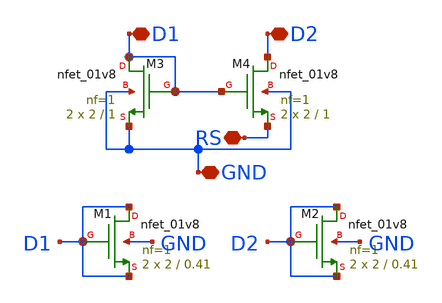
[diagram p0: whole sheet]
** sch_path: block2/xschem/block2.sch
**.subckt block2 RS D1 D2 GND
*.iopin RS
*.iopin D1
*.iopin D2
*.iopin GND
XM3 D1 D1 GND GND sky130_fd_pr__nfet_01v8 L=1 W=2 nf=1 ad='int((nf+1)/2) * W/nf * 0.29' as='int((nf+2)/2) * W/nf * 0.29'
+ pd='2*int((nf+1)/2) * (W/nf + 0.29)' ps='2*int((nf+2)/2) * (W/nf + 0.29)' nrd='0.29 / W' nrs='0.29 / W'
+ sa=0 sb=0 sd=0 mult=2 m=2
XM4 D2 D1 RS GND sky130_fd_pr__nfet_01v8 L=1 W=2 nf=1 ad='int((nf+1)/2) * W/nf * 0.29' as='int((nf+2)/2) * W/nf * 0.29'
+ pd='2*int((nf+1)/2) * (W/nf + 0.29)' ps='2*int((nf+2)/2) * (W/nf + 0.29)' nrd='0.29 / W' nrs='0.29 / W'
+ sa=0 sb=0 sd=0 mult=2 m=2
XM1 D1 D1 D1 GND sky130_fd_pr__nfet_01v8 L=0.41 W=2 nf=1 ad='int((nf+1)/2) * W/nf * 0.29' as='int((nf+2)/2) * W/nf * 0.29'
+ pd='2*int((nf+1)/2) * (W/nf + 0.29)' ps='2*int((nf+2)/2) * (W/nf + 0.29)' nrd='0.29 / W' nrs='0.29 / W'
+ sa=0 sb=0 sd=0 mult=2 m=2
XM2 D2 D2 D2 GND sky130_fd_pr__nfet_01v8 L=0.41 W=2 nf=1 ad='int((nf+1)/2) * W/nf * 0.29' as='int((nf+2)/2) * W/nf * 0.29'
+ pd='2*int((nf+1)/2) * (W/nf + 0.29)' ps='2*int((nf+2)/2) * (W/nf + 0.29)' nrd='0.29 / W' nrs='0.29 / W'
+ sa=0 sb=0 sd=0 mult=2 m=2
**.ends
.end
